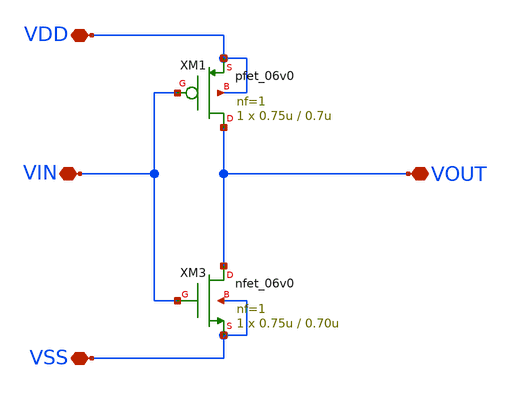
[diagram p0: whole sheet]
** sch_path: xschem/hv_inverter_W075L070.sch
* SPDX-FileCopyrightText: 2026 Clyde laforge <clyde.laforge@cern.ch>
* SPDX-License-Identifier: CERN-OHL-W-2.0
**.subckt hv_inverter_W075L070 VDD VSS VIN VOUT
*.iopin VDD
*.iopin VSS
*.iopin VIN
*.iopin VOUT
XM3 VOUT VIN VSS VSS nfet_06v0 L=0.70u W=0.75u nf=1 ad='int((nf+1)/2) * W/nf * 0.18u' as='int((nf+2)/2) * W/nf * 0.18u'
+ pd='2*int((nf+1)/2) * (W/nf + 0.18u)' ps='2*int((nf+2)/2) * (W/nf + 0.18u)' nrd='0.18u / W' nrs='0.18u / W'
+ sa=0 sb=0 sd=0 m=1
XM1 VOUT VIN VDD VDD pfet_06v0 L=0.7u W=0.75u nf=1 ad='int((nf+1)/2) * W/nf * 0.18u' as='int((nf+2)/2) * W/nf * 0.18u'
+ pd='2*int((nf+1)/2) * (W/nf + 0.18u)' ps='2*int((nf+2)/2) * (W/nf + 0.18u)' nrd='0.18u / W' nrs='0.18u / W'
+ sa=0 sb=0 sd=0 m=1
**.ends
.end
